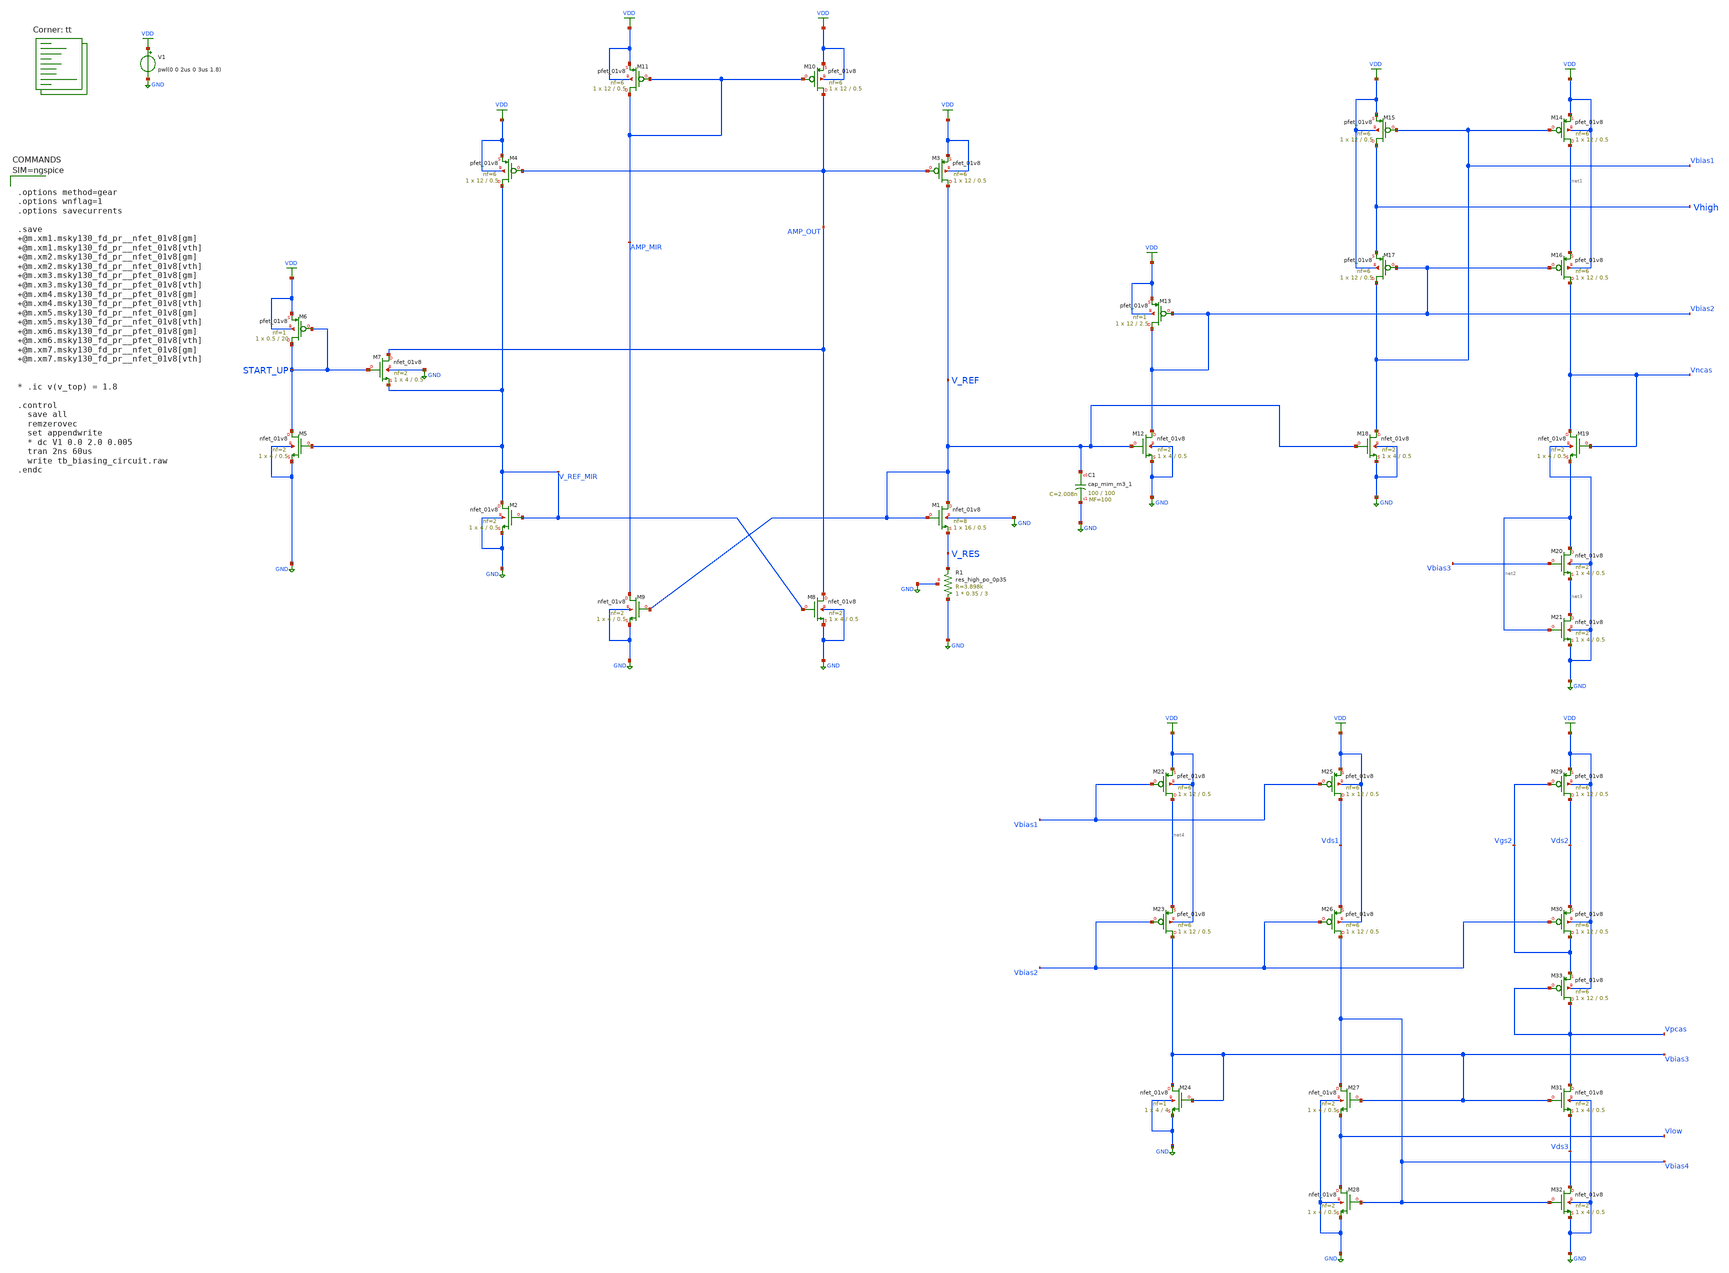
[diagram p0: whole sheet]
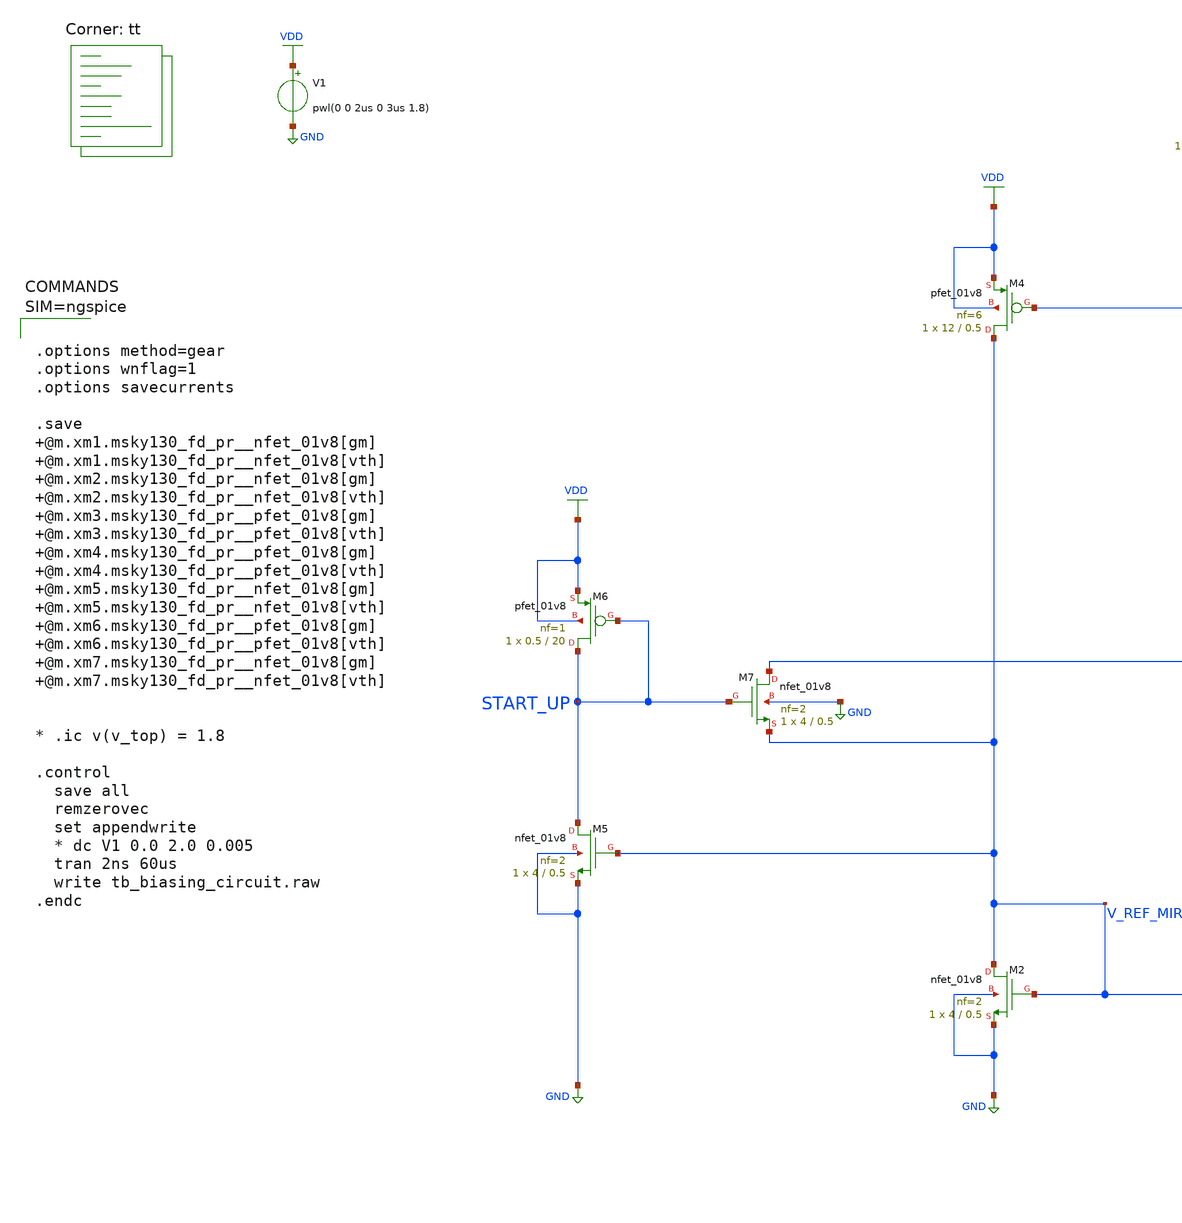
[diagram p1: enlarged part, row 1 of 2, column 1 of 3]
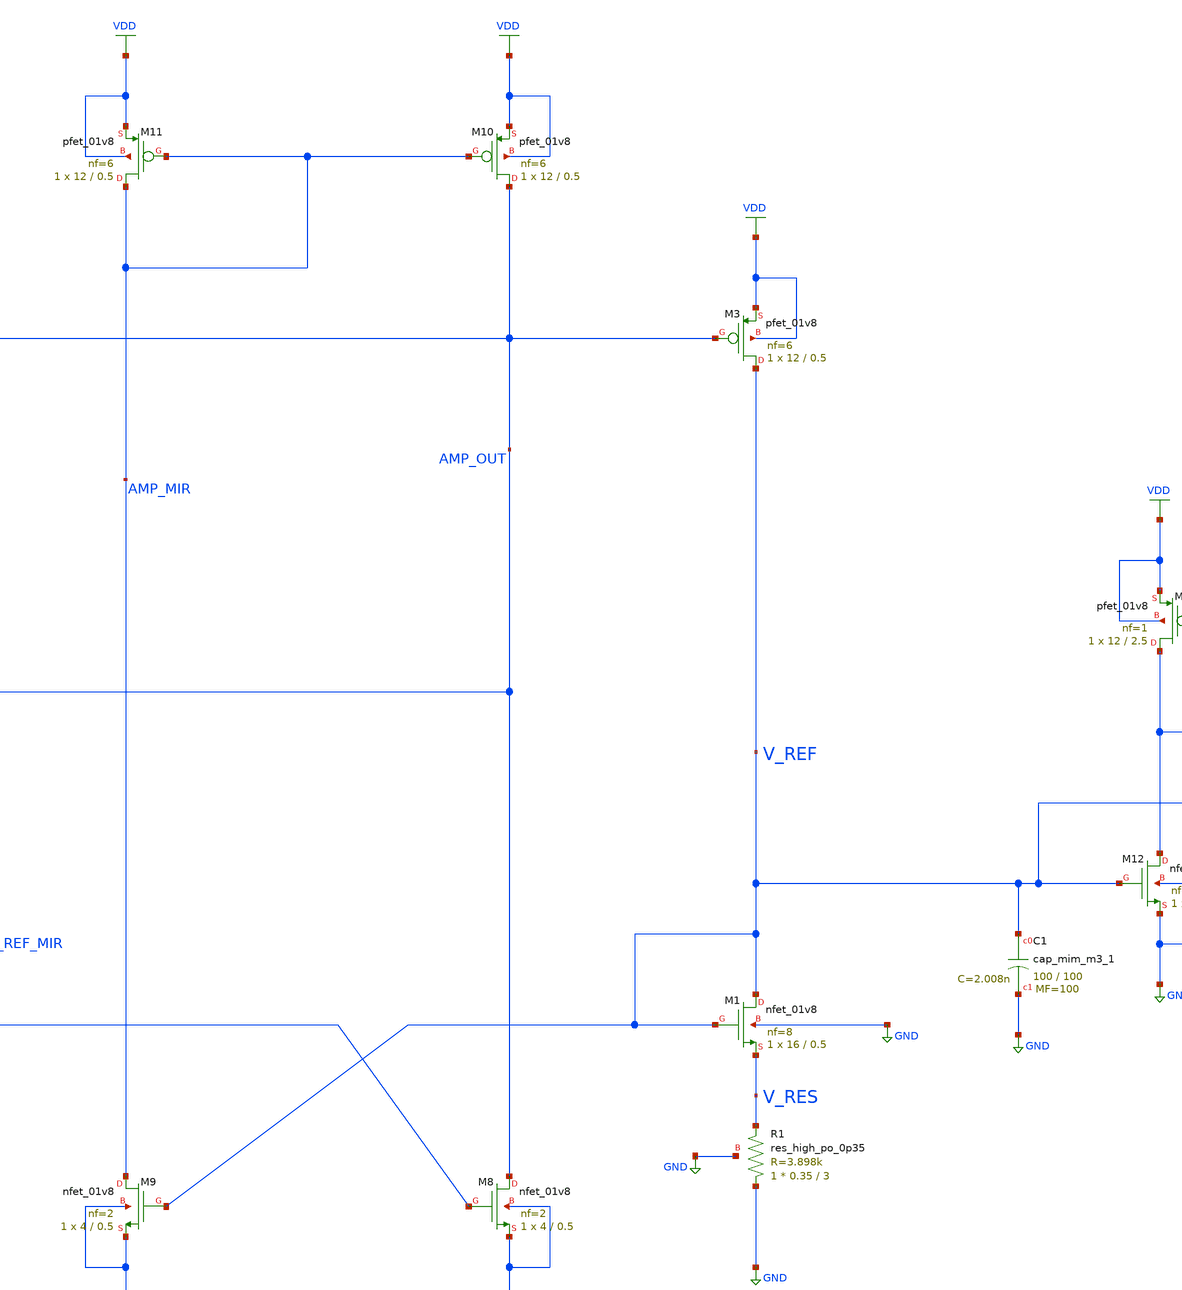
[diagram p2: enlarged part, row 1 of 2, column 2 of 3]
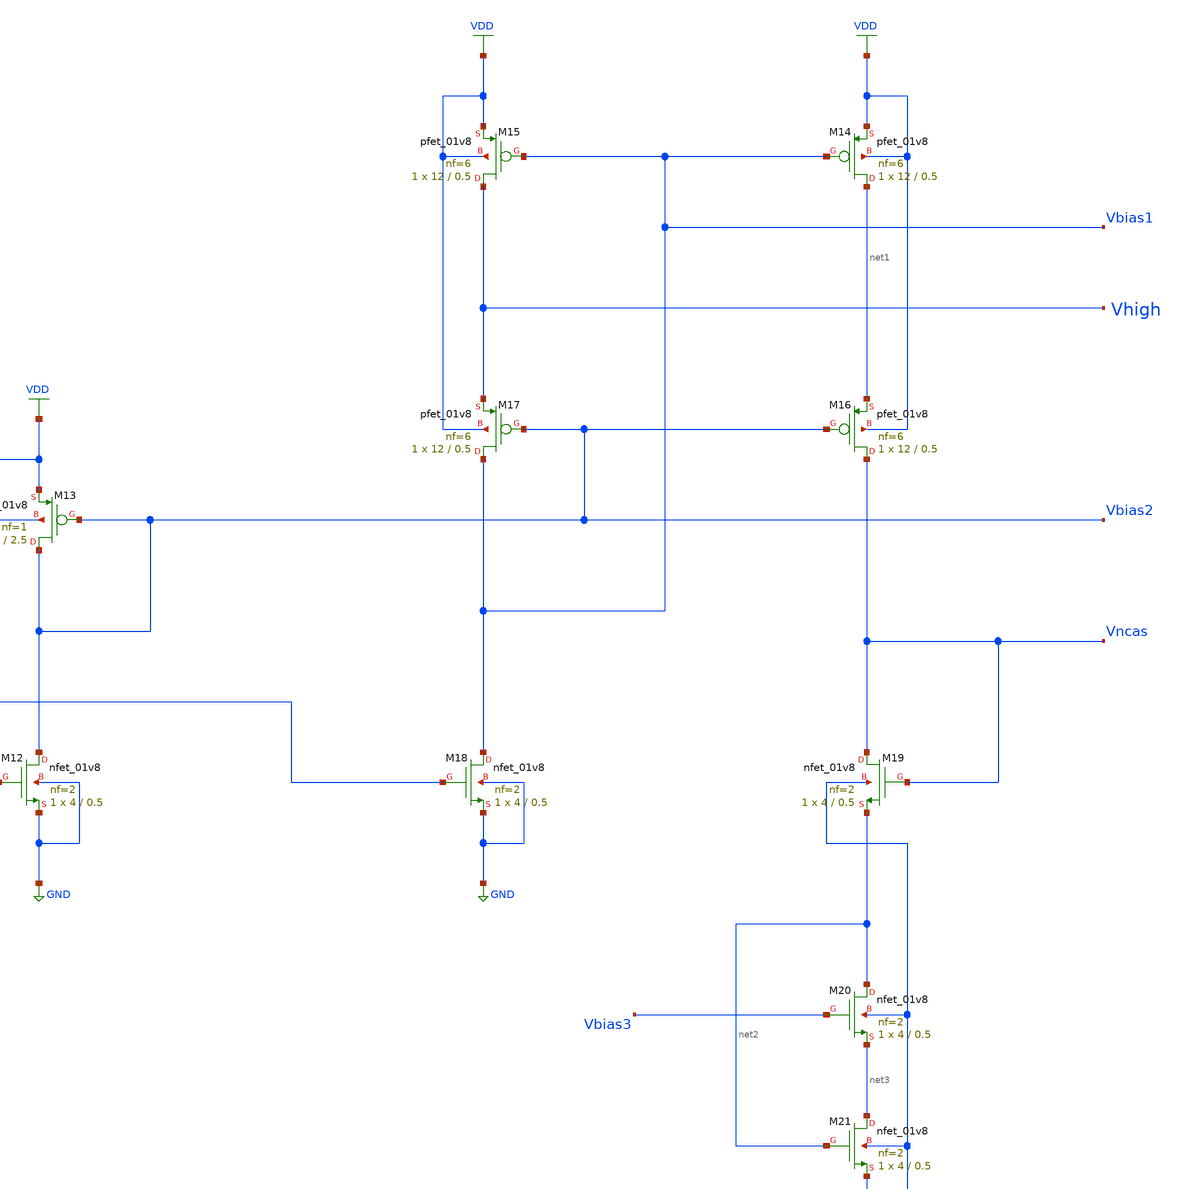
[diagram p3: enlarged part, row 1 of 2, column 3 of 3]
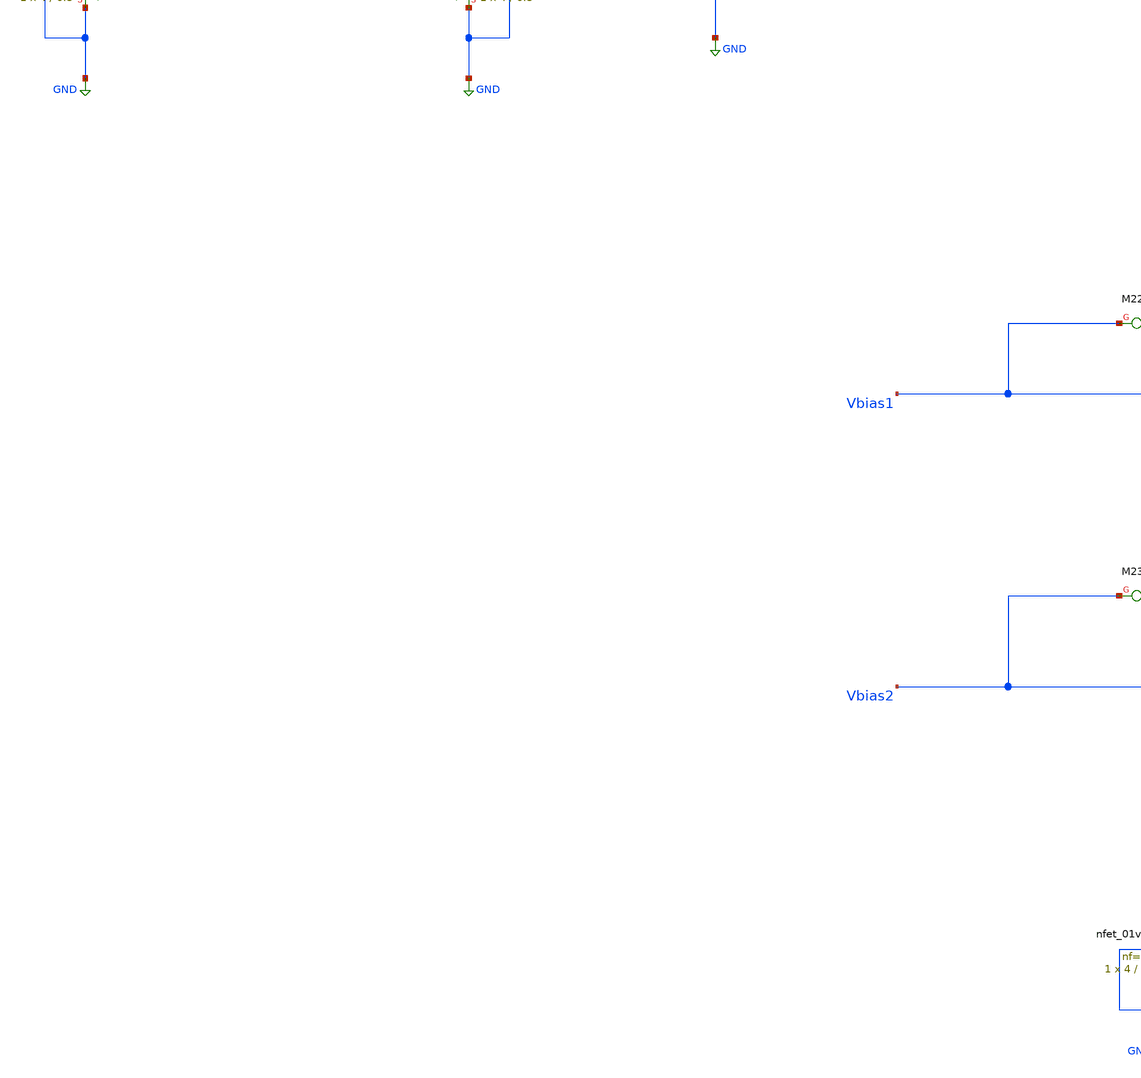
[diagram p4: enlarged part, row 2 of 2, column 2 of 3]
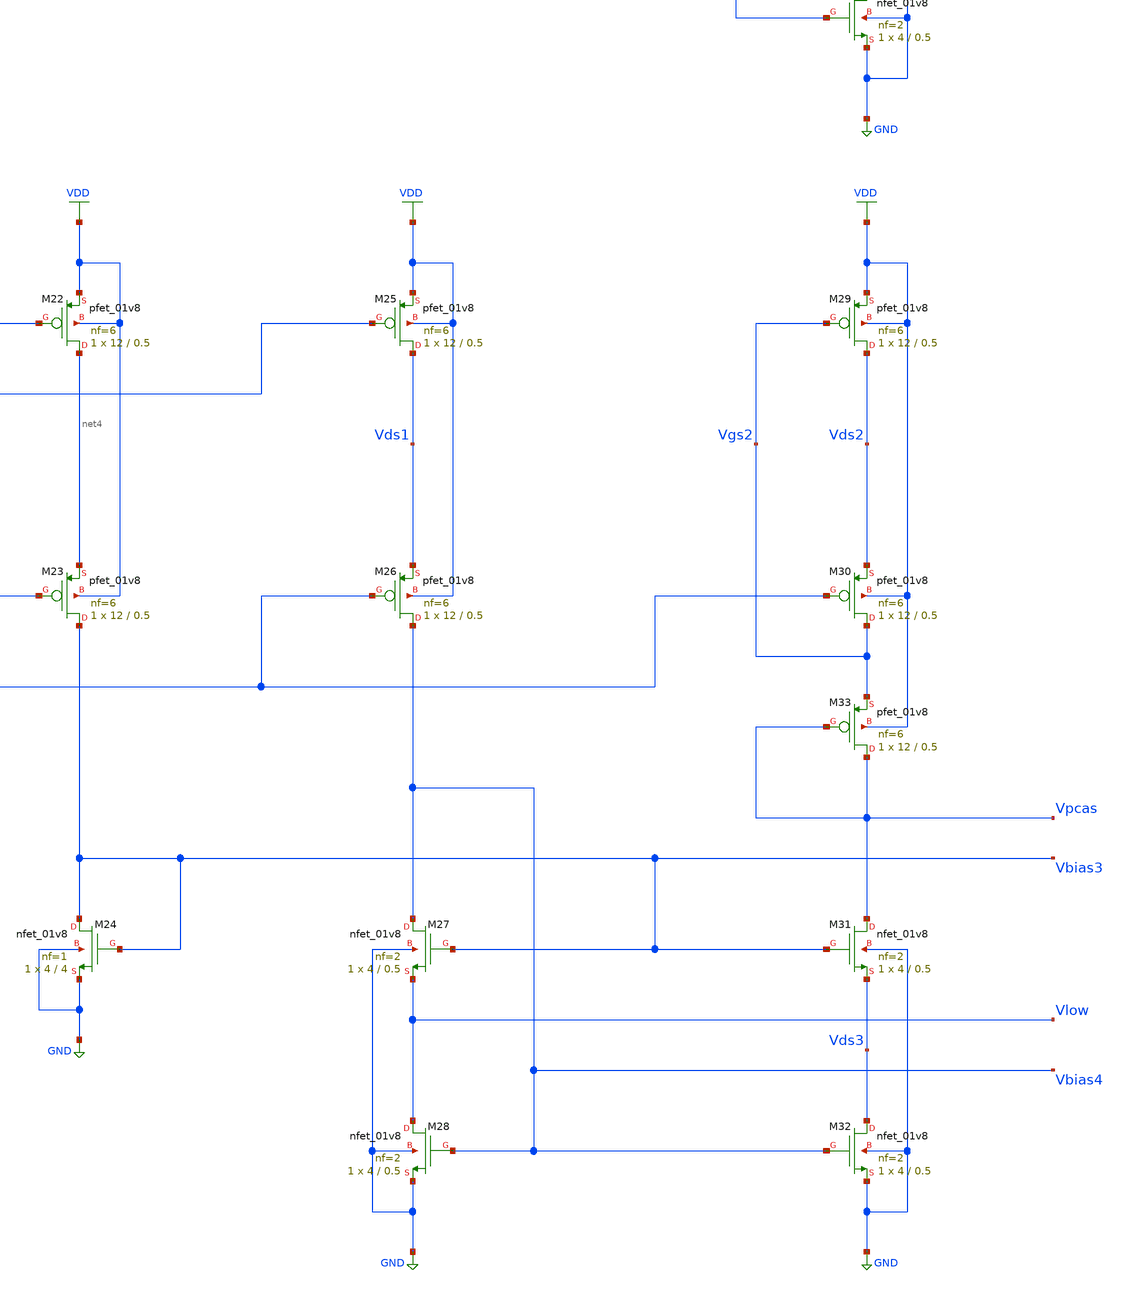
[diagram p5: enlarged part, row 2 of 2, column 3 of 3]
** sch_path: projects/ASU/EEE572/schematic/tb_biasing_circuit.sch
**.subckt tb_biasing_circuit
V1 VDD GND pwl(0 0 2us 0 3us 1.8)
XM1 V_REF V_REF V_RES GND sky130_fd_pr__nfet_01v8 L=0.5 W=16 nf=8 ad='int((nf+1)/2) * W/nf * 0.29' as='int((nf+2)/2) * W/nf * 0.29'
+ pd='2*int((nf+1)/2) * (W/nf + 0.29)' ps='2*int((nf+2)/2) * (W/nf + 0.29)' nrd='0.29 / W' nrs='0.29 / W'
+ sa=0 sb=0 sd=0 mult=1 m=1
XM2 V_REF_MIR V_REF_MIR GND GND sky130_fd_pr__nfet_01v8 L=0.5 W=4 nf=2 ad='int((nf+1)/2) * W/nf * 0.29'
+ as='int((nf+2)/2) * W/nf * 0.29' pd='2*int((nf+1)/2) * (W/nf + 0.29)' ps='2*int((nf+2)/2) * (W/nf + 0.29)'
+ nrd='0.29 / W' nrs='0.29 / W' sa=0 sb=0 sd=0 mult=1 m=1
XM5 START_UP V_REF_MIR GND GND sky130_fd_pr__nfet_01v8 L=0.5 W=4 nf=2 ad='int((nf+1)/2) * W/nf * 0.29'
+ as='int((nf+2)/2) * W/nf * 0.29' pd='2*int((nf+1)/2) * (W/nf + 0.29)' ps='2*int((nf+2)/2) * (W/nf + 0.29)'
+ nrd='0.29 / W' nrs='0.29 / W' sa=0 sb=0 sd=0 mult=1 m=1
XM7 AMP_OUT START_UP V_REF_MIR GND sky130_fd_pr__nfet_01v8 L=0.5 W=4 nf=2 ad='int((nf+1)/2) * W/nf * 0.29'
+ as='int((nf+2)/2) * W/nf * 0.29' pd='2*int((nf+1)/2) * (W/nf + 0.29)' ps='2*int((nf+2)/2) * (W/nf + 0.29)'
+ nrd='0.29 / W' nrs='0.29 / W' sa=0 sb=0 sd=0 mult=1 m=1
XR1 GND V_RES GND sky130_fd_pr__res_high_po_0p35 L=3 mult=1 m=1
XM6 START_UP START_UP VDD VDD sky130_fd_pr__pfet_01v8 L=20 W=0.5 nf=1 ad='int((nf+1)/2) * W/nf * 0.29'
+ as='int((nf+2)/2) * W/nf * 0.29' pd='2*int((nf+1)/2) * (W/nf + 0.29)' ps='2*int((nf+2)/2) * (W/nf + 0.29)'
+ nrd='0.29 / W' nrs='0.29 / W' sa=0 sb=0 sd=0 mult=1 m=1
XM3 V_REF AMP_OUT VDD VDD sky130_fd_pr__pfet_01v8 L=0.5 W=12 nf=6 ad='int((nf+1)/2) * W/nf * 0.29' as='int((nf+2)/2) * W/nf * 0.29'
+ pd='2*int((nf+1)/2) * (W/nf + 0.29)' ps='2*int((nf+2)/2) * (W/nf + 0.29)' nrd='0.29 / W' nrs='0.29 / W'
+ sa=0 sb=0 sd=0 mult=1 m=1
XM4 V_REF_MIR AMP_OUT VDD VDD sky130_fd_pr__pfet_01v8 L=0.5 W=12 nf=6 ad='int((nf+1)/2) * W/nf * 0.29'
+ as='int((nf+2)/2) * W/nf * 0.29' pd='2*int((nf+1)/2) * (W/nf + 0.29)' ps='2*int((nf+2)/2) * (W/nf + 0.29)'
+ nrd='0.29 / W' nrs='0.29 / W' sa=0 sb=0 sd=0 mult=1 m=1
XM8 AMP_OUT V_REF_MIR GND GND sky130_fd_pr__nfet_01v8 L=0.5 W=4 nf=2 ad='int((nf+1)/2) * W/nf * 0.29'
+ as='int((nf+2)/2) * W/nf * 0.29' pd='2*int((nf+1)/2) * (W/nf + 0.29)' ps='2*int((nf+2)/2) * (W/nf + 0.29)'
+ nrd='0.29 / W' nrs='0.29 / W' sa=0 sb=0 sd=0 mult=1 m=1
XM9 AMP_MIR V_REF GND GND sky130_fd_pr__nfet_01v8 L=0.5 W=4 nf=2 ad='int((nf+1)/2) * W/nf * 0.29' as='int((nf+2)/2) * W/nf * 0.29'
+ pd='2*int((nf+1)/2) * (W/nf + 0.29)' ps='2*int((nf+2)/2) * (W/nf + 0.29)' nrd='0.29 / W' nrs='0.29 / W'
+ sa=0 sb=0 sd=0 mult=1 m=1
XM10 AMP_OUT AMP_MIR VDD VDD sky130_fd_pr__pfet_01v8 L=0.5 W=12 nf=6 ad='int((nf+1)/2) * W/nf * 0.29'
+ as='int((nf+2)/2) * W/nf * 0.29' pd='2*int((nf+1)/2) * (W/nf + 0.29)' ps='2*int((nf+2)/2) * (W/nf + 0.29)'
+ nrd='0.29 / W' nrs='0.29 / W' sa=0 sb=0 sd=0 mult=1 m=1
XM11 AMP_MIR AMP_MIR VDD VDD sky130_fd_pr__pfet_01v8 L=0.5 W=12 nf=6 ad='int((nf+1)/2) * W/nf * 0.29'
+ as='int((nf+2)/2) * W/nf * 0.29' pd='2*int((nf+1)/2) * (W/nf + 0.29)' ps='2*int((nf+2)/2) * (W/nf + 0.29)'
+ nrd='0.29 / W' nrs='0.29 / W' sa=0 sb=0 sd=0 mult=1 m=1
XM12 Vbias2 V_REF GND GND sky130_fd_pr__nfet_01v8 L=0.5 W=4 nf=2 ad='int((nf+1)/2) * W/nf * 0.29' as='int((nf+2)/2) * W/nf * 0.29'
+ pd='2*int((nf+1)/2) * (W/nf + 0.29)' ps='2*int((nf+2)/2) * (W/nf + 0.29)' nrd='0.29 / W' nrs='0.29 / W'
+ sa=0 sb=0 sd=0 mult=1 m=1
XM13 Vbias2 Vbias2 VDD VDD sky130_fd_pr__pfet_01v8 L=2.5 W=12 nf=1 ad='int((nf+1)/2) * W/nf * 0.29' as='int((nf+2)/2) * W/nf * 0.29'
+ pd='2*int((nf+1)/2) * (W/nf + 0.29)' ps='2*int((nf+2)/2) * (W/nf + 0.29)' nrd='0.29 / W' nrs='0.29 / W'
+ sa=0 sb=0 sd=0 mult=1 m=1
XM14 net1 Vbias1 VDD VDD sky130_fd_pr__pfet_01v8 L=0.5 W=12 nf=6 ad='int((nf+1)/2) * W/nf * 0.29' as='int((nf+2)/2) * W/nf * 0.29'
+ pd='2*int((nf+1)/2) * (W/nf + 0.29)' ps='2*int((nf+2)/2) * (W/nf + 0.29)' nrd='0.29 / W' nrs='0.29 / W'
+ sa=0 sb=0 sd=0 mult=1 m=1
XM15 Vhigh Vbias1 VDD VDD sky130_fd_pr__pfet_01v8 L=0.5 W=12 nf=6 ad='int((nf+1)/2) * W/nf * 0.29' as='int((nf+2)/2) * W/nf * 0.29'
+ pd='2*int((nf+1)/2) * (W/nf + 0.29)' ps='2*int((nf+2)/2) * (W/nf + 0.29)' nrd='0.29 / W' nrs='0.29 / W'
+ sa=0 sb=0 sd=0 mult=1 m=1
XM16 Vncas Vbias2 net1 VDD sky130_fd_pr__pfet_01v8 L=0.5 W=12 nf=6 ad='int((nf+1)/2) * W/nf * 0.29' as='int((nf+2)/2) * W/nf * 0.29'
+ pd='2*int((nf+1)/2) * (W/nf + 0.29)' ps='2*int((nf+2)/2) * (W/nf + 0.29)' nrd='0.29 / W' nrs='0.29 / W'
+ sa=0 sb=0 sd=0 mult=1 m=1
XM17 Vbias1 Vbias2 Vhigh VDD sky130_fd_pr__pfet_01v8 L=0.5 W=12 nf=6 ad='int((nf+1)/2) * W/nf * 0.29'
+ as='int((nf+2)/2) * W/nf * 0.29' pd='2*int((nf+1)/2) * (W/nf + 0.29)' ps='2*int((nf+2)/2) * (W/nf + 0.29)'
+ nrd='0.29 / W' nrs='0.29 / W' sa=0 sb=0 sd=0 mult=1 m=1
XM18 Vbias1 V_REF GND GND sky130_fd_pr__nfet_01v8 L=0.5 W=4 nf=2 ad='int((nf+1)/2) * W/nf * 0.29' as='int((nf+2)/2) * W/nf * 0.29'
+ pd='2*int((nf+1)/2) * (W/nf + 0.29)' ps='2*int((nf+2)/2) * (W/nf + 0.29)' nrd='0.29 / W' nrs='0.29 / W'
+ sa=0 sb=0 sd=0 mult=1 m=1
XM19 Vncas Vncas net2 GND sky130_fd_pr__nfet_01v8 L=0.5 W=4 nf=2 ad='int((nf+1)/2) * W/nf * 0.29' as='int((nf+2)/2) * W/nf * 0.29'
+ pd='2*int((nf+1)/2) * (W/nf + 0.29)' ps='2*int((nf+2)/2) * (W/nf + 0.29)' nrd='0.29 / W' nrs='0.29 / W'
+ sa=0 sb=0 sd=0 mult=1 m=1
XM20 net2 Vbias3 net3 GND sky130_fd_pr__nfet_01v8 L=0.5 W=4 nf=2 ad='int((nf+1)/2) * W/nf * 0.29' as='int((nf+2)/2) * W/nf * 0.29'
+ pd='2*int((nf+1)/2) * (W/nf + 0.29)' ps='2*int((nf+2)/2) * (W/nf + 0.29)' nrd='0.29 / W' nrs='0.29 / W'
+ sa=0 sb=0 sd=0 mult=1 m=1
XM21 net3 net2 GND GND sky130_fd_pr__nfet_01v8 L=0.5 W=4 nf=2 ad='int((nf+1)/2) * W/nf * 0.29' as='int((nf+2)/2) * W/nf * 0.29'
+ pd='2*int((nf+1)/2) * (W/nf + 0.29)' ps='2*int((nf+2)/2) * (W/nf + 0.29)' nrd='0.29 / W' nrs='0.29 / W'
+ sa=0 sb=0 sd=0 mult=1 m=1
XM22 net4 Vbias1 VDD VDD sky130_fd_pr__pfet_01v8 L=0.5 W=12 nf=6 ad='int((nf+1)/2) * W/nf * 0.29' as='int((nf+2)/2) * W/nf * 0.29'
+ pd='2*int((nf+1)/2) * (W/nf + 0.29)' ps='2*int((nf+2)/2) * (W/nf + 0.29)' nrd='0.29 / W' nrs='0.29 / W'
+ sa=0 sb=0 sd=0 mult=1 m=1
XM23 Vbias3 Vbias2 net4 VDD sky130_fd_pr__pfet_01v8 L=0.5 W=12 nf=6 ad='int((nf+1)/2) * W/nf * 0.29'
+ as='int((nf+2)/2) * W/nf * 0.29' pd='2*int((nf+1)/2) * (W/nf + 0.29)' ps='2*int((nf+2)/2) * (W/nf + 0.29)'
+ nrd='0.29 / W' nrs='0.29 / W' sa=0 sb=0 sd=0 mult=1 m=1
XM24 Vbias3 Vbias3 GND GND sky130_fd_pr__nfet_01v8 L=4 W=4 nf=1 ad='int((nf+1)/2) * W/nf * 0.29' as='int((nf+2)/2) * W/nf * 0.29'
+ pd='2*int((nf+1)/2) * (W/nf + 0.29)' ps='2*int((nf+2)/2) * (W/nf + 0.29)' nrd='0.29 / W' nrs='0.29 / W'
+ sa=0 sb=0 sd=0 mult=1 m=1
XM25 Vds1 Vbias1 VDD VDD sky130_fd_pr__pfet_01v8 L=0.5 W=12 nf=6 ad='int((nf+1)/2) * W/nf * 0.29' as='int((nf+2)/2) * W/nf * 0.29'
+ pd='2*int((nf+1)/2) * (W/nf + 0.29)' ps='2*int((nf+2)/2) * (W/nf + 0.29)' nrd='0.29 / W' nrs='0.29 / W'
+ sa=0 sb=0 sd=0 mult=1 m=1
XM26 Vbias4 Vbias2 Vds1 VDD sky130_fd_pr__pfet_01v8 L=0.5 W=12 nf=6 ad='int((nf+1)/2) * W/nf * 0.29'
+ as='int((nf+2)/2) * W/nf * 0.29' pd='2*int((nf+1)/2) * (W/nf + 0.29)' ps='2*int((nf+2)/2) * (W/nf + 0.29)'
+ nrd='0.29 / W' nrs='0.29 / W' sa=0 sb=0 sd=0 mult=1 m=1
XM27 Vbias4 Vbias3 Vlow GND sky130_fd_pr__nfet_01v8 L=0.5 W=4 nf=2 ad='int((nf+1)/2) * W/nf * 0.29' as='int((nf+2)/2) * W/nf * 0.29'
+ pd='2*int((nf+1)/2) * (W/nf + 0.29)' ps='2*int((nf+2)/2) * (W/nf + 0.29)' nrd='0.29 / W' nrs='0.29 / W'
+ sa=0 sb=0 sd=0 mult=1 m=1
XM28 Vlow Vbias4 GND GND sky130_fd_pr__nfet_01v8 L=0.5 W=4 nf=2 ad='int((nf+1)/2) * W/nf * 0.29' as='int((nf+2)/2) * W/nf * 0.29'
+ pd='2*int((nf+1)/2) * (W/nf + 0.29)' ps='2*int((nf+2)/2) * (W/nf + 0.29)' nrd='0.29 / W' nrs='0.29 / W'
+ sa=0 sb=0 sd=0 mult=1 m=1
XM29 Vds2 Vgs2 VDD VDD sky130_fd_pr__pfet_01v8 L=0.5 W=12 nf=6 ad='int((nf+1)/2) * W/nf * 0.29' as='int((nf+2)/2) * W/nf * 0.29'
+ pd='2*int((nf+1)/2) * (W/nf + 0.29)' ps='2*int((nf+2)/2) * (W/nf + 0.29)' nrd='0.29 / W' nrs='0.29 / W'
+ sa=0 sb=0 sd=0 mult=1 m=1
XM30 Vgs2 Vbias2 Vds2 VDD sky130_fd_pr__pfet_01v8 L=0.5 W=12 nf=6 ad='int((nf+1)/2) * W/nf * 0.29' as='int((nf+2)/2) * W/nf * 0.29'
+ pd='2*int((nf+1)/2) * (W/nf + 0.29)' ps='2*int((nf+2)/2) * (W/nf + 0.29)' nrd='0.29 / W' nrs='0.29 / W'
+ sa=0 sb=0 sd=0 mult=1 m=1
XM31 Vpcas Vbias3 Vds3 GND sky130_fd_pr__nfet_01v8 L=0.5 W=4 nf=2 ad='int((nf+1)/2) * W/nf * 0.29' as='int((nf+2)/2) * W/nf * 0.29'
+ pd='2*int((nf+1)/2) * (W/nf + 0.29)' ps='2*int((nf+2)/2) * (W/nf + 0.29)' nrd='0.29 / W' nrs='0.29 / W'
+ sa=0 sb=0 sd=0 mult=1 m=1
XM32 Vds3 Vbias4 GND GND sky130_fd_pr__nfet_01v8 L=0.5 W=4 nf=2 ad='int((nf+1)/2) * W/nf * 0.29' as='int((nf+2)/2) * W/nf * 0.29'
+ pd='2*int((nf+1)/2) * (W/nf + 0.29)' ps='2*int((nf+2)/2) * (W/nf + 0.29)' nrd='0.29 / W' nrs='0.29 / W'
+ sa=0 sb=0 sd=0 mult=1 m=1
XM33 Vpcas Vpcas Vgs2 VDD sky130_fd_pr__pfet_01v8 L=0.5 W=12 nf=6 ad='int((nf+1)/2) * W/nf * 0.29' as='int((nf+2)/2) * W/nf * 0.29'
+ pd='2*int((nf+1)/2) * (W/nf + 0.29)' ps='2*int((nf+2)/2) * (W/nf + 0.29)' nrd='0.29 / W' nrs='0.29 / W'
+ sa=0 sb=0 sd=0 mult=1 m=1
XC1 V_REF GND sky130_fd_pr__cap_mim_m3_1 W=100 L=100 MF=100 m=100
**** begin user architecture code
.lib $::SKYWATER_MODELS/sky130.lib.spice tt



.options method=gear
.options wnflag=1
.options savecurrents

.save @m.xm1.msky130_fd_pr__nfet_01v8[gm] @m.xm1.msky130_fd_pr__nfet_01v8[vth] @m.xm2.msky130_fd_pr__nfet_01v8[gm] @m.xm2.msky130_fd_pr__nfet_01v8[vth] @m.xm3.msky130_fd_pr__pfet_01v8[gm] @m.xm3.msky130_fd_pr__pfet_01v8[vth] @m.xm4.msky130_fd_pr__pfet_01v8[gm] @m.xm4.msky130_fd_pr__pfet_01v8[vth] @m.xm5.msky130_fd_pr__nfet_01v8[gm] @m.xm5.msky130_fd_pr__nfet_01v8[vth] @m.xm6.msky130_fd_pr__pfet_01v8[gm] @m.xm6.msky130_fd_pr__pfet_01v8[vth] @m.xm7.msky130_fd_pr__nfet_01v8[gm] @m.xm7.msky130_fd_pr__nfet_01v8[vth]


* .ic v(v_top) = 1.8

.control
  save all
  remzerovec
  set appendwrite
  * dc V1 0.0 2.0 0.005
  tran 2ns 60us
  write tb_biasing_circuit.raw
.endc





**** end user architecture code
**.ends
.GLOBAL GND
.GLOBAL VDD
.end
